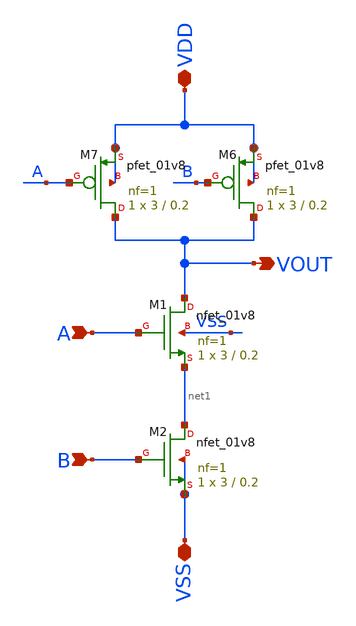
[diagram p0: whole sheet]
** sch_path: Xschem/PLL_TOP_Schematics/NAND_1.sch
**.subckt NAND_1 VDD VSS A B VOUT
*.iopin VDD
*.iopin VSS
*.ipin A
*.ipin B
*.opin VOUT
XM1 VOUT A net1 VSS sky130_fd_pr__nfet_01v8 L=0.2 W=3 nf=1 ad='int((nf+1)/2) * W/nf * 0.29' as='int((nf+2)/2) * W/nf * 0.29'
+ pd='2*int((nf+1)/2) * (W/nf + 0.29)' ps='2*int((nf+2)/2) * (W/nf + 0.29)' nrd='0.29 / W' nrs='0.29 / W'
+ sa=0 sb=0 sd=0 mult=1 m=1
XM2 net1 B VSS VSS sky130_fd_pr__nfet_01v8 L=0.2 W=3 nf=1 ad='int((nf+1)/2) * W/nf * 0.29' as='int((nf+2)/2) * W/nf * 0.29'
+ pd='2*int((nf+1)/2) * (W/nf + 0.29)' ps='2*int((nf+2)/2) * (W/nf + 0.29)' nrd='0.29 / W' nrs='0.29 / W'
+ sa=0 sb=0 sd=0 mult=1 m=1
XM6 VOUT B VDD VDD sky130_fd_pr__pfet_01v8 L=0.2 W=3 nf=1 ad='int((nf+1)/2) * W/nf * 0.29' as='int((nf+2)/2) * W/nf * 0.29'
+ pd='2*int((nf+1)/2) * (W/nf + 0.29)' ps='2*int((nf+2)/2) * (W/nf + 0.29)' nrd='0.29 / W' nrs='0.29 / W'
+ sa=0 sb=0 sd=0 mult=1 m=1
XM7 VOUT A VDD VDD sky130_fd_pr__pfet_01v8 L=0.2 W=3 nf=1 ad='int((nf+1)/2) * W/nf * 0.29' as='int((nf+2)/2) * W/nf * 0.29'
+ pd='2*int((nf+1)/2) * (W/nf + 0.29)' ps='2*int((nf+2)/2) * (W/nf + 0.29)' nrd='0.29 / W' nrs='0.29 / W'
+ sa=0 sb=0 sd=0 mult=1 m=1
**.ends
.end
